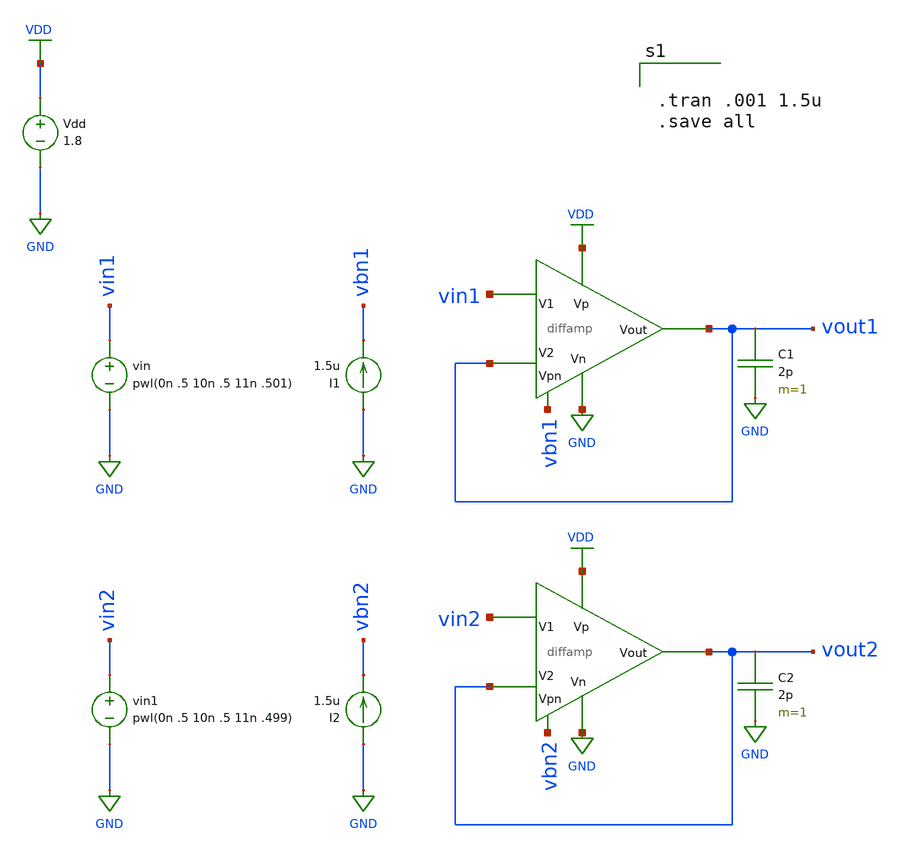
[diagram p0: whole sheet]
** sch_path: mini_proj_3/schematic/diff_2e.sch
**.subckt diff_2e
Vdd VDD GND 1.8
vin vin1 GND pwl(0n .5 10n .5 11n .501)
I1 GND vbn1 1.5u
C1 vout1 GND 2p m=1
X1 vbn1 VDD GND vin1 vout1 vout1 diffamp
C2 vout2 GND 2p m=1
X2 vbn2 VDD GND vin2 vout2 vout2 diffamp
vin1 vin2 GND pwl(0n .5 10n .5 11n .499)
I2 GND vbn2 1.5u
**** begin user architecture code

.option wnflag=1
.lib ~/skywater/skywater-pdk/libraries/sky130_fd_pr_ngspice/latest/models/sky130.lib.spice tt



.tran .001 1.5u
.save all


**** end user architecture code
**.ends
.GLOBAL VDD
.GLOBAL GND
.end
